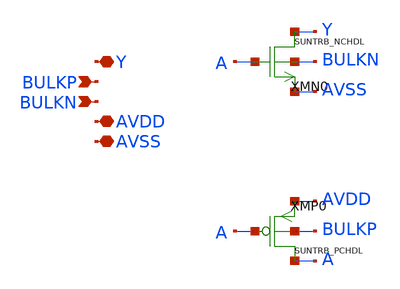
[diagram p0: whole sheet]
** sch_path: design/SUN_TRB_SKY130NM/SUNTRB_TIEL_CV.sch
**.subckt SUNTRB_TIEL_CV Y BULKP BULKN AVDD AVSS
*.iopin Y
*.ipin BULKP
*.ipin BULKN
*.iopin AVDD
*.iopin AVSS
XMN0 Y A AVSS BULKN SUNTRB_NCHDL xoffset=0 yoffset=0 angle=0
XMP0 A A AVDD BULKP SUNTRB_PCHDL xoffset=0 yoffset=0 angle=0 M=1
**.ends
.end
